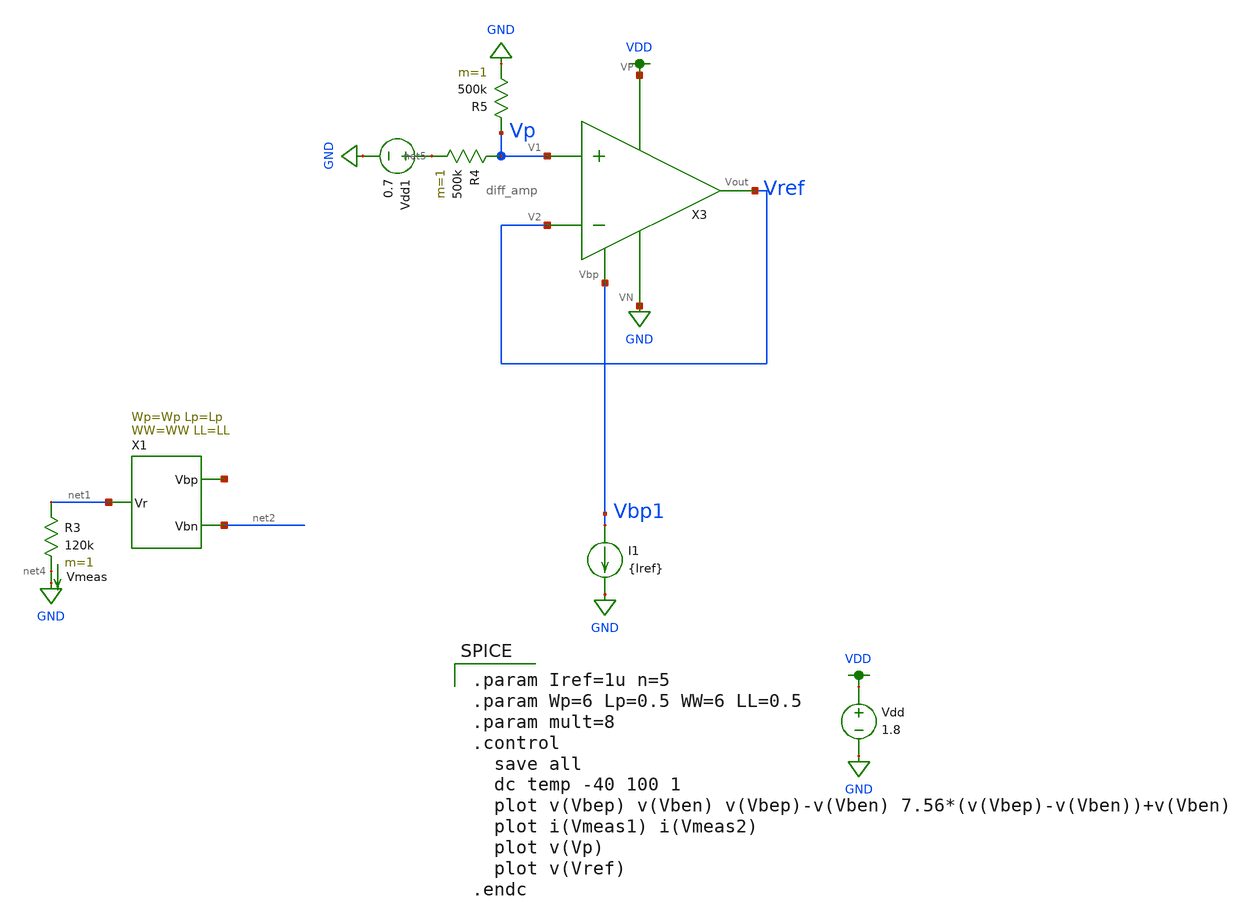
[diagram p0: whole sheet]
** sch_path: schematic/test/difference_amp.sch
**.subckt difference_amp
Vdd VDD GND 1.8
X1 net1 net2 net3 ibias Wp=Wp Lp=Lp WW=WW LL=LL
R3 net1 net4 120k m=1
Vmeas net4 GND 0
.save i(vmeas)
X3 VDD Vbp1 Vref Vp Vref GND diff_amp
R4 Vp net5 500k m=1
R5 Vp GND 500k m=1
Vdd1 net5 GND 0.7
I1 Vbp1 GND {Iref}
**** begin user architecture code

.option wnflag=1
.param MC_SWITCH=0.0
.lib /media/qdeng/526448C32060CF5C/skywater/skywater-pdk/libraries/sky130_fd_pr_ngspice/latest/models/sky130.lib.spice tt


.param Iref=1u n=5
.param Wp=6 Lp=0.5 WW=6 LL=0.5
.param mult=8
.control
  save all
  dc temp -40 100 1
  plot v(Vbep) v(Vben) v(Vbep)-v(Vben) 7.56*(v(Vbep)-v(Vben))+v(Vben)
  plot i(Vmeas1) i(Vmeas2)
  plot v(Vp)
  plot v(Vref)
.endc

**** end user architecture code
**.ends
.GLOBAL GND
.GLOBAL VDD
.end
